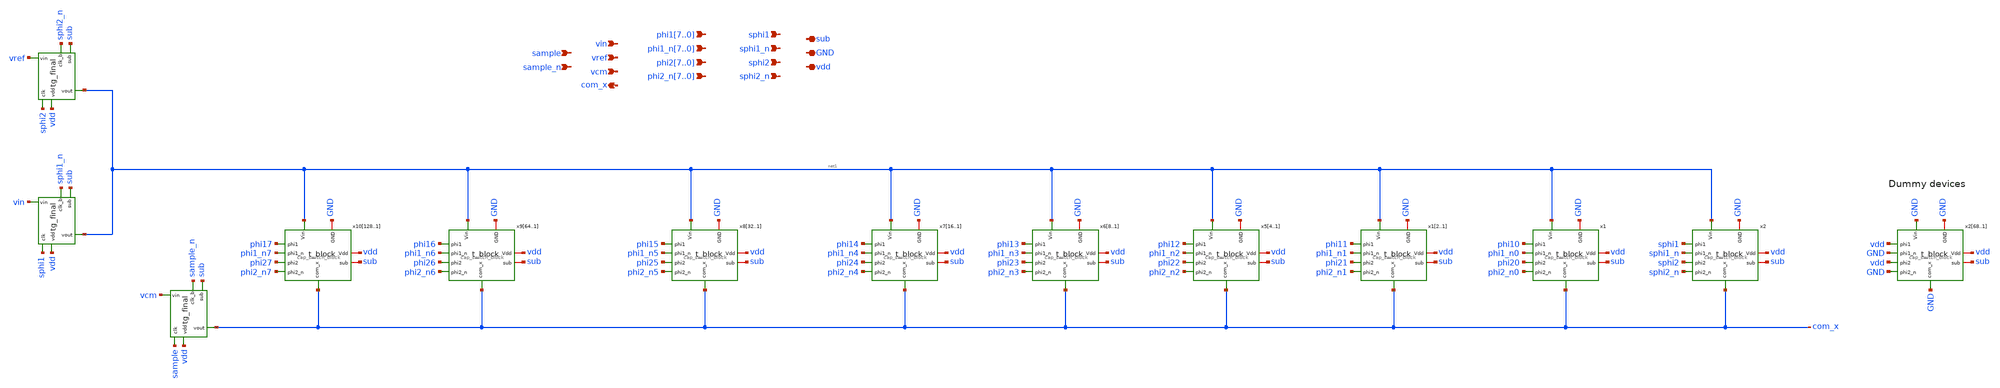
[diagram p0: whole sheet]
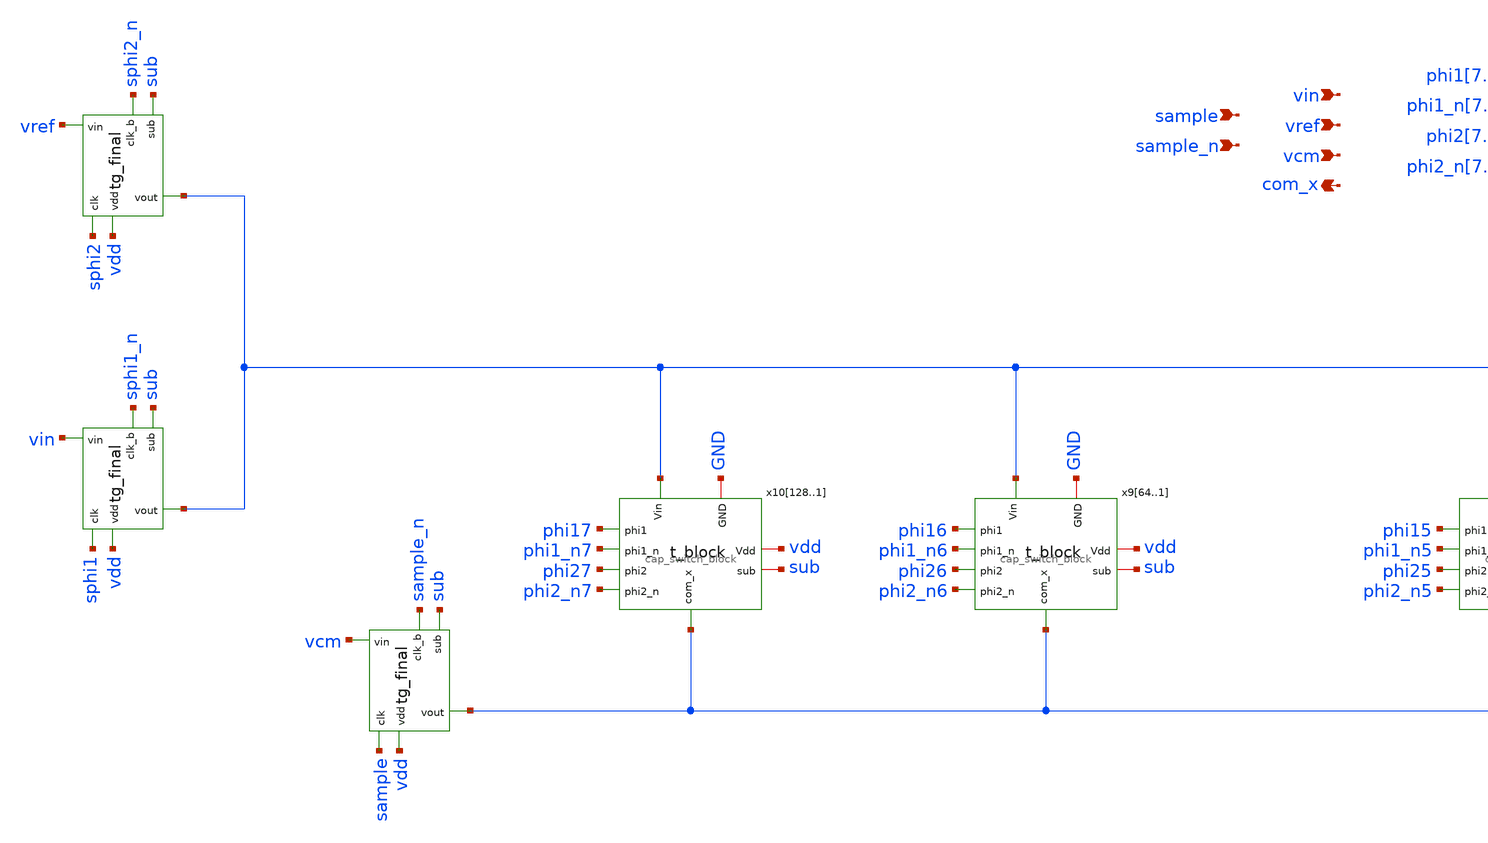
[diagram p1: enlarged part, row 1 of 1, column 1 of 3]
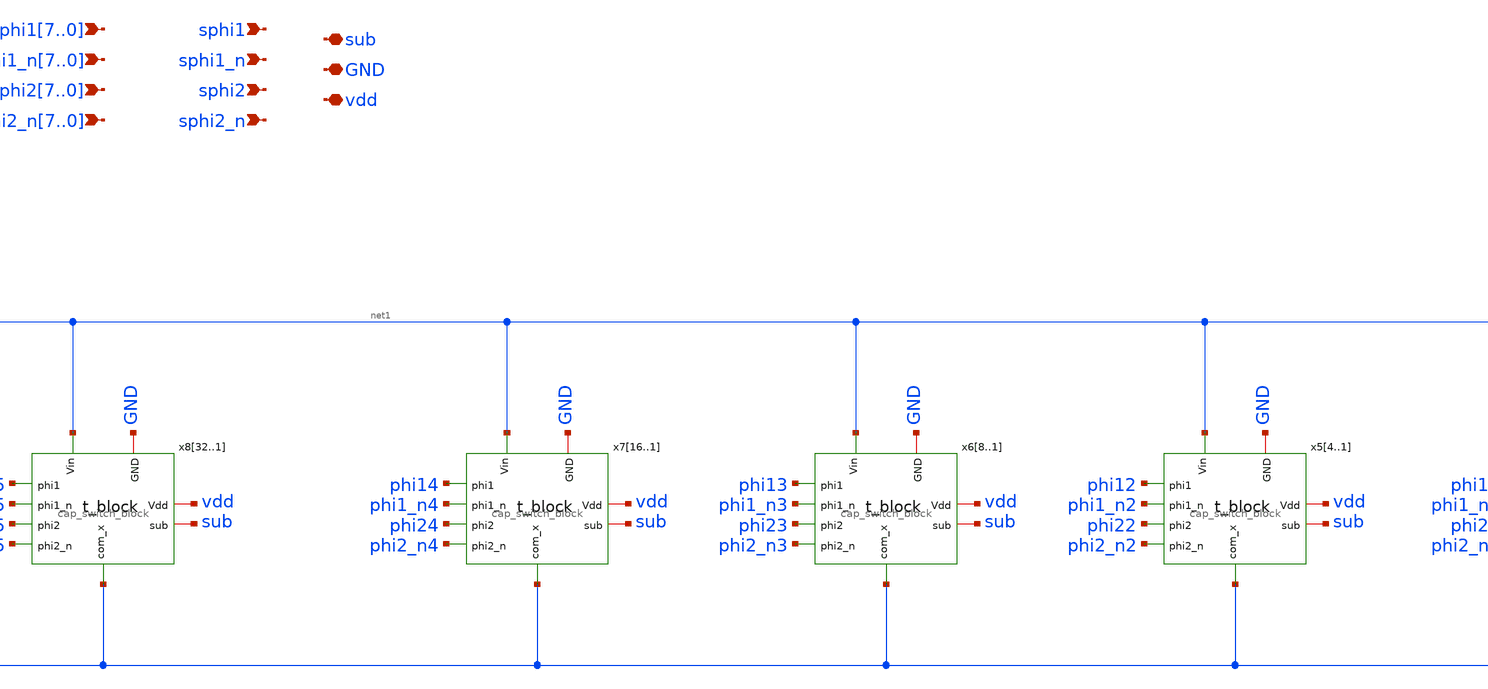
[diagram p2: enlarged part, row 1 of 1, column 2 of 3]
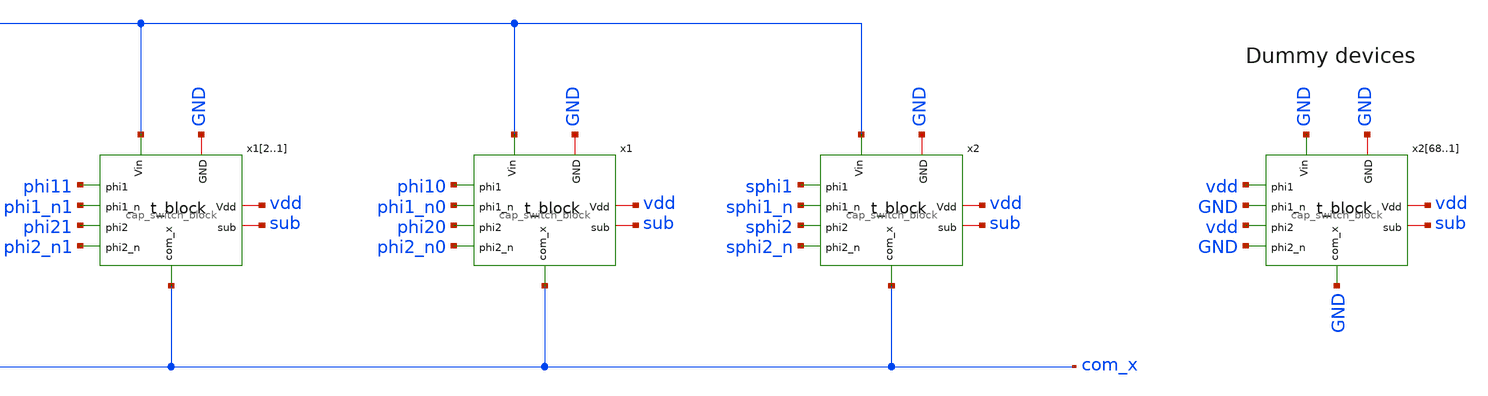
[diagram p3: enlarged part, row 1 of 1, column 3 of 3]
** sch_path: top/test/design/capdac_p.sch
**.subckt capdac_p phi17,phi16,phi15,phi14,phi13,phi12,phi11,phi10
*+ phi1_n7,phi1_n6,phi1_n5,phi1_n4,phi1_n3,phi1_n2,phi1_n1,phi1_n0 vdd GND sub phi27,phi26,phi25,phi24,phi23,phi22,phi21,phi20
*+ phi2_n7,phi2_n6,phi2_n5,phi2_n4,phi2_n3,phi2_n2,phi2_n1,phi2_n0 com_x sphi1 sphi1_n sphi2 sphi2_n vcm vref vin sample_n sample
*.ipin phi17,phi16,phi15,phi14,phi13,phi12,phi11,phi10
*.ipin phi1_n7,phi1_n6,phi1_n5,phi1_n4,phi1_n3,phi1_n2,phi1_n1,phi1_n0
*.iopin vdd
*.iopin GND
*.iopin sub
*.ipin phi27,phi26,phi25,phi24,phi23,phi22,phi21,phi20
*.ipin phi2_n7,phi2_n6,phi2_n5,phi2_n4,phi2_n3,phi2_n2,phi2_n1,phi2_n0
*.opin com_x
*.ipin sphi1
*.ipin sphi1_n
*.ipin sphi2
*.ipin sphi2_n
*.ipin vcm
*.ipin vref
*.ipin vin
*.ipin sample_n
*.ipin sample
x2 net1 sub GND vdd sphi1 sphi2 sphi2_n sphi1_n com_x cap_switch_block
x1 net1 sub GND vdd phi10 phi20 phi2_n0 phi1_n0 com_x cap_switch_block
x12 net1 sub GND vdd phi11 phi21 phi2_n1 phi1_n1 com_x cap_switch_block
x11 net1 sub GND vdd phi11 phi21 phi2_n1 phi1_n1 com_x cap_switch_block
x54 net1 sub GND vdd phi12 phi22 phi2_n2 phi1_n2 com_x cap_switch_block
x53 net1 sub GND vdd phi12 phi22 phi2_n2 phi1_n2 com_x cap_switch_block
x52 net1 sub GND vdd phi12 phi22 phi2_n2 phi1_n2 com_x cap_switch_block
x51 net1 sub GND vdd phi12 phi22 phi2_n2 phi1_n2 com_x cap_switch_block
x68 net1 sub GND vdd phi13 phi23 phi2_n3 phi1_n3 com_x cap_switch_block
x67 net1 sub GND vdd phi13 phi23 phi2_n3 phi1_n3 com_x cap_switch_block
x66 net1 sub GND vdd phi13 phi23 phi2_n3 phi1_n3 com_x cap_switch_block
x65 net1 sub GND vdd phi13 phi23 phi2_n3 phi1_n3 com_x cap_switch_block
x64 net1 sub GND vdd phi13 phi23 phi2_n3 phi1_n3 com_x cap_switch_block
x63 net1 sub GND vdd phi13 phi23 phi2_n3 phi1_n3 com_x cap_switch_block
x62 net1 sub GND vdd phi13 phi23 phi2_n3 phi1_n3 com_x cap_switch_block
x61 net1 sub GND vdd phi13 phi23 phi2_n3 phi1_n3 com_x cap_switch_block
x716 net1 sub GND vdd phi14 phi24 phi2_n4 phi1_n4 com_x cap_switch_block
x715 net1 sub GND vdd phi14 phi24 phi2_n4 phi1_n4 com_x cap_switch_block
x714 net1 sub GND vdd phi14 phi24 phi2_n4 phi1_n4 com_x cap_switch_block
x713 net1 sub GND vdd phi14 phi24 phi2_n4 phi1_n4 com_x cap_switch_block
x712 net1 sub GND vdd phi14 phi24 phi2_n4 phi1_n4 com_x cap_switch_block
x711 net1 sub GND vdd phi14 phi24 phi2_n4 phi1_n4 com_x cap_switch_block
x710 net1 sub GND vdd phi14 phi24 phi2_n4 phi1_n4 com_x cap_switch_block
x79 net1 sub GND vdd phi14 phi24 phi2_n4 phi1_n4 com_x cap_switch_block
x78 net1 sub GND vdd phi14 phi24 phi2_n4 phi1_n4 com_x cap_switch_block
x77 net1 sub GND vdd phi14 phi24 phi2_n4 phi1_n4 com_x cap_switch_block
x76 net1 sub GND vdd phi14 phi24 phi2_n4 phi1_n4 com_x cap_switch_block
x75 net1 sub GND vdd phi14 phi24 phi2_n4 phi1_n4 com_x cap_switch_block
x74 net1 sub GND vdd phi14 phi24 phi2_n4 phi1_n4 com_x cap_switch_block
x73 net1 sub GND vdd phi14 phi24 phi2_n4 phi1_n4 com_x cap_switch_block
x72 net1 sub GND vdd phi14 phi24 phi2_n4 phi1_n4 com_x cap_switch_block
x71 net1 sub GND vdd phi14 phi24 phi2_n4 phi1_n4 com_x cap_switch_block
x832 net1 sub GND vdd phi15 phi25 phi2_n5 phi1_n5 com_x cap_switch_block
x831 net1 sub GND vdd phi15 phi25 phi2_n5 phi1_n5 com_x cap_switch_block
x830 net1 sub GND vdd phi15 phi25 phi2_n5 phi1_n5 com_x cap_switch_block
x829 net1 sub GND vdd phi15 phi25 phi2_n5 phi1_n5 com_x cap_switch_block
x828 net1 sub GND vdd phi15 phi25 phi2_n5 phi1_n5 com_x cap_switch_block
x827 net1 sub GND vdd phi15 phi25 phi2_n5 phi1_n5 com_x cap_switch_block
x826 net1 sub GND vdd phi15 phi25 phi2_n5 phi1_n5 com_x cap_switch_block
x825 net1 sub GND vdd phi15 phi25 phi2_n5 phi1_n5 com_x cap_switch_block
x824 net1 sub GND vdd phi15 phi25 phi2_n5 phi1_n5 com_x cap_switch_block
x823 net1 sub GND vdd phi15 phi25 phi2_n5 phi1_n5 com_x cap_switch_block
x822 net1 sub GND vdd phi15 phi25 phi2_n5 phi1_n5 com_x cap_switch_block
x821 net1 sub GND vdd phi15 phi25 phi2_n5 phi1_n5 com_x cap_switch_block
x820 net1 sub GND vdd phi15 phi25 phi2_n5 phi1_n5 com_x cap_switch_block
x819 net1 sub GND vdd phi15 phi25 phi2_n5 phi1_n5 com_x cap_switch_block
x818 net1 sub GND vdd phi15 phi25 phi2_n5 phi1_n5 com_x cap_switch_block
x817 net1 sub GND vdd phi15 phi25 phi2_n5 phi1_n5 com_x cap_switch_block
x816 net1 sub GND vdd phi15 phi25 phi2_n5 phi1_n5 com_x cap_switch_block
x815 net1 sub GND vdd phi15 phi25 phi2_n5 phi1_n5 com_x cap_switch_block
x814 net1 sub GND vdd phi15 phi25 phi2_n5 phi1_n5 com_x cap_switch_block
x813 net1 sub GND vdd phi15 phi25 phi2_n5 phi1_n5 com_x cap_switch_block
x812 net1 sub GND vdd phi15 phi25 phi2_n5 phi1_n5 com_x cap_switch_block
x811 net1 sub GND vdd phi15 phi25 phi2_n5 phi1_n5 com_x cap_switch_block
x810 net1 sub GND vdd phi15 phi25 phi2_n5 phi1_n5 com_x cap_switch_block
x89 net1 sub GND vdd phi15 phi25 phi2_n5 phi1_n5 com_x cap_switch_block
x88 net1 sub GND vdd phi15 phi25 phi2_n5 phi1_n5 com_x cap_switch_block
x87 net1 sub GND vdd phi15 phi25 phi2_n5 phi1_n5 com_x cap_switch_block
x86 net1 sub GND vdd phi15 phi25 phi2_n5 phi1_n5 com_x cap_switch_block
x85 net1 sub GND vdd phi15 phi25 phi2_n5 phi1_n5 com_x cap_switch_block
x84 net1 sub GND vdd phi15 phi25 phi2_n5 phi1_n5 com_x cap_switch_block
x83 net1 sub GND vdd phi15 phi25 phi2_n5 phi1_n5 com_x cap_switch_block
x82 net1 sub GND vdd phi15 phi25 phi2_n5 phi1_n5 com_x cap_switch_block
x81 net1 sub GND vdd phi15 phi25 phi2_n5 phi1_n5 com_x cap_switch_block
x964 net1 sub GND vdd phi16 phi26 phi2_n6 phi1_n6 com_x cap_switch_block
x963 net1 sub GND vdd phi16 phi26 phi2_n6 phi1_n6 com_x cap_switch_block
x962 net1 sub GND vdd phi16 phi26 phi2_n6 phi1_n6 com_x cap_switch_block
x961 net1 sub GND vdd phi16 phi26 phi2_n6 phi1_n6 com_x cap_switch_block
x960 net1 sub GND vdd phi16 phi26 phi2_n6 phi1_n6 com_x cap_switch_block
x959 net1 sub GND vdd phi16 phi26 phi2_n6 phi1_n6 com_x cap_switch_block
x958 net1 sub GND vdd phi16 phi26 phi2_n6 phi1_n6 com_x cap_switch_block
x957 net1 sub GND vdd phi16 phi26 phi2_n6 phi1_n6 com_x cap_switch_block
x956 net1 sub GND vdd phi16 phi26 phi2_n6 phi1_n6 com_x cap_switch_block
x955 net1 sub GND vdd phi16 phi26 phi2_n6 phi1_n6 com_x cap_switch_block
x954 net1 sub GND vdd phi16 phi26 phi2_n6 phi1_n6 com_x cap_switch_block
x953 net1 sub GND vdd phi16 phi26 phi2_n6 phi1_n6 com_x cap_switch_block
x952 net1 sub GND vdd phi16 phi26 phi2_n6 phi1_n6 com_x cap_switch_block
x951 net1 sub GND vdd phi16 phi26 phi2_n6 phi1_n6 com_x cap_switch_block
x950 net1 sub GND vdd phi16 phi26 phi2_n6 phi1_n6 com_x cap_switch_block
x949 net1 sub GND vdd phi16 phi26 phi2_n6 phi1_n6 com_x cap_switch_block
x948 net1 sub GND vdd phi16 phi26 phi2_n6 phi1_n6 com_x cap_switch_block
x947 net1 sub GND vdd phi16 phi26 phi2_n6 phi1_n6 com_x cap_switch_block
x946 net1 sub GND vdd phi16 phi26 phi2_n6 phi1_n6 com_x cap_switch_block
x945 net1 sub GND vdd phi16 phi26 phi2_n6 phi1_n6 com_x cap_switch_block
x944 net1 sub GND vdd phi16 phi26 phi2_n6 phi1_n6 com_x cap_switch_block
x943 net1 sub GND vdd phi16 phi26 phi2_n6 phi1_n6 com_x cap_switch_block
x942 net1 sub GND vdd phi16 phi26 phi2_n6 phi1_n6 com_x cap_switch_block
x941 net1 sub GND vdd phi16 phi26 phi2_n6 phi1_n6 com_x cap_switch_block
x940 net1 sub GND vdd phi16 phi26 phi2_n6 phi1_n6 com_x cap_switch_block
x939 net1 sub GND vdd phi16 phi26 phi2_n6 phi1_n6 com_x cap_switch_block
x938 net1 sub GND vdd phi16 phi26 phi2_n6 phi1_n6 com_x cap_switch_block
x937 net1 sub GND vdd phi16 phi26 phi2_n6 phi1_n6 com_x cap_switch_block
x936 net1 sub GND vdd phi16 phi26 phi2_n6 phi1_n6 com_x cap_switch_block
x935 net1 sub GND vdd phi16 phi26 phi2_n6 phi1_n6 com_x cap_switch_block
x934 net1 sub GND vdd phi16 phi26 phi2_n6 phi1_n6 com_x cap_switch_block
x933 net1 sub GND vdd phi16 phi26 phi2_n6 phi1_n6 com_x cap_switch_block
x932 net1 sub GND vdd phi16 phi26 phi2_n6 phi1_n6 com_x cap_switch_block
x931 net1 sub GND vdd phi16 phi26 phi2_n6 phi1_n6 com_x cap_switch_block
x930 net1 sub GND vdd phi16 phi26 phi2_n6 phi1_n6 com_x cap_switch_block
x929 net1 sub GND vdd phi16 phi26 phi2_n6 phi1_n6 com_x cap_switch_block
x928 net1 sub GND vdd phi16 phi26 phi2_n6 phi1_n6 com_x cap_switch_block
x927 net1 sub GND vdd phi16 phi26 phi2_n6 phi1_n6 com_x cap_switch_block
x926 net1 sub GND vdd phi16 phi26 phi2_n6 phi1_n6 com_x cap_switch_block
x925 net1 sub GND vdd phi16 phi26 phi2_n6 phi1_n6 com_x cap_switch_block
x924 net1 sub GND vdd phi16 phi26 phi2_n6 phi1_n6 com_x cap_switch_block
x923 net1 sub GND vdd phi16 phi26 phi2_n6 phi1_n6 com_x cap_switch_block
x922 net1 sub GND vdd phi16 phi26 phi2_n6 phi1_n6 com_x cap_switch_block
x921 net1 sub GND vdd phi16 phi26 phi2_n6 phi1_n6 com_x cap_switch_block
x920 net1 sub GND vdd phi16 phi26 phi2_n6 phi1_n6 com_x cap_switch_block
x919 net1 sub GND vdd phi16 phi26 phi2_n6 phi1_n6 com_x cap_switch_block
x918 net1 sub GND vdd phi16 phi26 phi2_n6 phi1_n6 com_x cap_switch_block
x917 net1 sub GND vdd phi16 phi26 phi2_n6 phi1_n6 com_x cap_switch_block
x916 net1 sub GND vdd phi16 phi26 phi2_n6 phi1_n6 com_x cap_switch_block
x915 net1 sub GND vdd phi16 phi26 phi2_n6 phi1_n6 com_x cap_switch_block
x914 net1 sub GND vdd phi16 phi26 phi2_n6 phi1_n6 com_x cap_switch_block
x913 net1 sub GND vdd phi16 phi26 phi2_n6 phi1_n6 com_x cap_switch_block
x912 net1 sub GND vdd phi16 phi26 phi2_n6 phi1_n6 com_x cap_switch_block
x911 net1 sub GND vdd phi16 phi26 phi2_n6 phi1_n6 com_x cap_switch_block
x910 net1 sub GND vdd phi16 phi26 phi2_n6 phi1_n6 com_x cap_switch_block
x99 net1 sub GND vdd phi16 phi26 phi2_n6 phi1_n6 com_x cap_switch_block
x98 net1 sub GND vdd phi16 phi26 phi2_n6 phi1_n6 com_x cap_switch_block
x97 net1 sub GND vdd phi16 phi26 phi2_n6 phi1_n6 com_x cap_switch_block
x96 net1 sub GND vdd phi16 phi26 phi2_n6 phi1_n6 com_x cap_switch_block
x95 net1 sub GND vdd phi16 phi26 phi2_n6 phi1_n6 com_x cap_switch_block
x94 net1 sub GND vdd phi16 phi26 phi2_n6 phi1_n6 com_x cap_switch_block
x93 net1 sub GND vdd phi16 phi26 phi2_n6 phi1_n6 com_x cap_switch_block
x92 net1 sub GND vdd phi16 phi26 phi2_n6 phi1_n6 com_x cap_switch_block
x91 net1 sub GND vdd phi16 phi26 phi2_n6 phi1_n6 com_x cap_switch_block
x10128 net1 sub GND vdd phi17 phi27 phi2_n7 phi1_n7 com_x cap_switch_block
x10127 net1 sub GND vdd phi17 phi27 phi2_n7 phi1_n7 com_x cap_switch_block
x10126 net1 sub GND vdd phi17 phi27 phi2_n7 phi1_n7 com_x cap_switch_block
x10125 net1 sub GND vdd phi17 phi27 phi2_n7 phi1_n7 com_x cap_switch_block
x10124 net1 sub GND vdd phi17 phi27 phi2_n7 phi1_n7 com_x cap_switch_block
x10123 net1 sub GND vdd phi17 phi27 phi2_n7 phi1_n7 com_x cap_switch_block
x10122 net1 sub GND vdd phi17 phi27 phi2_n7 phi1_n7 com_x cap_switch_block
x10121 net1 sub GND vdd phi17 phi27 phi2_n7 phi1_n7 com_x cap_switch_block
x10120 net1 sub GND vdd phi17 phi27 phi2_n7 phi1_n7 com_x cap_switch_block
x10119 net1 sub GND vdd phi17 phi27 phi2_n7 phi1_n7 com_x cap_switch_block
x10118 net1 sub GND vdd phi17 phi27 phi2_n7 phi1_n7 com_x cap_switch_block
x10117 net1 sub GND vdd phi17 phi27 phi2_n7 phi1_n7 com_x cap_switch_block
x10116 net1 sub GND vdd phi17 phi27 phi2_n7 phi1_n7 com_x cap_switch_block
x10115 net1 sub GND vdd phi17 phi27 phi2_n7 phi1_n7 com_x cap_switch_block
x10114 net1 sub GND vdd phi17 phi27 phi2_n7 phi1_n7 com_x cap_switch_block
x10113 net1 sub GND vdd phi17 phi27 phi2_n7 phi1_n7 com_x cap_switch_block
x10112 net1 sub GND vdd phi17 phi27 phi2_n7 phi1_n7 com_x cap_switch_block
x10111 net1 sub GND vdd phi17 phi27 phi2_n7 phi1_n7 com_x cap_switch_block
x10110 net1 sub GND vdd phi17 phi27 phi2_n7 phi1_n7 com_x cap_switch_block
x10109 net1 sub GND vdd phi17 phi27 phi2_n7 phi1_n7 com_x cap_switch_block
x10108 net1 sub GND vdd phi17 phi27 phi2_n7 phi1_n7 com_x cap_switch_block
x10107 net1 sub GND vdd phi17 phi27 phi2_n7 phi1_n7 com_x cap_switch_block
x10106 net1 sub GND vdd phi17 phi27 phi2_n7 phi1_n7 com_x cap_switch_block
x10105 net1 sub GND vdd phi17 phi27 phi2_n7 phi1_n7 com_x cap_switch_block
x10104 net1 sub GND vdd phi17 phi27 phi2_n7 phi1_n7 com_x cap_switch_block
x10103 net1 sub GND vdd phi17 phi27 phi2_n7 phi1_n7 com_x cap_switch_block
x10102 net1 sub GND vdd phi17 phi27 phi2_n7 phi1_n7 com_x cap_switch_block
x10101 net1 sub GND vdd phi17 phi27 phi2_n7 phi1_n7 com_x cap_switch_block
x10100 net1 sub GND vdd phi17 phi27 phi2_n7 phi1_n7 com_x cap_switch_block
x1099 net1 sub GND vdd phi17 phi27 phi2_n7 phi1_n7 com_x cap_switch_block
x1098 net1 sub GND vdd phi17 phi27 phi2_n7 phi1_n7 com_x cap_switch_block
x1097 net1 sub GND vdd phi17 phi27 phi2_n7 phi1_n7 com_x cap_switch_block
x1096 net1 sub GND vdd phi17 phi27 phi2_n7 phi1_n7 com_x cap_switch_block
x1095 net1 sub GND vdd phi17 phi27 phi2_n7 phi1_n7 com_x cap_switch_block
x1094 net1 sub GND vdd phi17 phi27 phi2_n7 phi1_n7 com_x cap_switch_block
x1093 net1 sub GND vdd phi17 phi27 phi2_n7 phi1_n7 com_x cap_switch_block
x1092 net1 sub GND vdd phi17 phi27 phi2_n7 phi1_n7 com_x cap_switch_block
x1091 net1 sub GND vdd phi17 phi27 phi2_n7 phi1_n7 com_x cap_switch_block
x1090 net1 sub GND vdd phi17 phi27 phi2_n7 phi1_n7 com_x cap_switch_block
x1089 net1 sub GND vdd phi17 phi27 phi2_n7 phi1_n7 com_x cap_switch_block
x1088 net1 sub GND vdd phi17 phi27 phi2_n7 phi1_n7 com_x cap_switch_block
x1087 net1 sub GND vdd phi17 phi27 phi2_n7 phi1_n7 com_x cap_switch_block
x1086 net1 sub GND vdd phi17 phi27 phi2_n7 phi1_n7 com_x cap_switch_block
x1085 net1 sub GND vdd phi17 phi27 phi2_n7 phi1_n7 com_x cap_switch_block
x1084 net1 sub GND vdd phi17 phi27 phi2_n7 phi1_n7 com_x cap_switch_block
x1083 net1 sub GND vdd phi17 phi27 phi2_n7 phi1_n7 com_x cap_switch_block
x1082 net1 sub GND vdd phi17 phi27 phi2_n7 phi1_n7 com_x cap_switch_block
x1081 net1 sub GND vdd phi17 phi27 phi2_n7 phi1_n7 com_x cap_switch_block
x1080 net1 sub GND vdd phi17 phi27 phi2_n7 phi1_n7 com_x cap_switch_block
x1079 net1 sub GND vdd phi17 phi27 phi2_n7 phi1_n7 com_x cap_switch_block
x1078 net1 sub GND vdd phi17 phi27 phi2_n7 phi1_n7 com_x cap_switch_block
x1077 net1 sub GND vdd phi17 phi27 phi2_n7 phi1_n7 com_x cap_switch_block
x1076 net1 sub GND vdd phi17 phi27 phi2_n7 phi1_n7 com_x cap_switch_block
x1075 net1 sub GND vdd phi17 phi27 phi2_n7 phi1_n7 com_x cap_switch_block
x1074 net1 sub GND vdd phi17 phi27 phi2_n7 phi1_n7 com_x cap_switch_block
x1073 net1 sub GND vdd phi17 phi27 phi2_n7 phi1_n7 com_x cap_switch_block
x1072 net1 sub GND vdd phi17 phi27 phi2_n7 phi1_n7 com_x cap_switch_block
x1071 net1 sub GND vdd phi17 phi27 phi2_n7 phi1_n7 com_x cap_switch_block
x1070 net1 sub GND vdd phi17 phi27 phi2_n7 phi1_n7 com_x cap_switch_block
x1069 net1 sub GND vdd phi17 phi27 phi2_n7 phi1_n7 com_x cap_switch_block
x1068 net1 sub GND vdd phi17 phi27 phi2_n7 phi1_n7 com_x cap_switch_block
x1067 net1 sub GND vdd phi17 phi27 phi2_n7 phi1_n7 com_x cap_switch_block
x1066 net1 sub GND vdd phi17 phi27 phi2_n7 phi1_n7 com_x cap_switch_block
x1065 net1 sub GND vdd phi17 phi27 phi2_n7 phi1_n7 com_x cap_switch_block
x1064 net1 sub GND vdd phi17 phi27 phi2_n7 phi1_n7 com_x cap_switch_block
x1063 net1 sub GND vdd phi17 phi27 phi2_n7 phi1_n7 com_x cap_switch_block
x1062 net1 sub GND vdd phi17 phi27 phi2_n7 phi1_n7 com_x cap_switch_block
x1061 net1 sub GND vdd phi17 phi27 phi2_n7 phi1_n7 com_x cap_switch_block
x1060 net1 sub GND vdd phi17 phi27 phi2_n7 phi1_n7 com_x cap_switch_block
x1059 net1 sub GND vdd phi17 phi27 phi2_n7 phi1_n7 com_x cap_switch_block
x1058 net1 sub GND vdd phi17 phi27 phi2_n7 phi1_n7 com_x cap_switch_block
x1057 net1 sub GND vdd phi17 phi27 phi2_n7 phi1_n7 com_x cap_switch_block
x1056 net1 sub GND vdd phi17 phi27 phi2_n7 phi1_n7 com_x cap_switch_block
x1055 net1 sub GND vdd phi17 phi27 phi2_n7 phi1_n7 com_x cap_switch_block
x1054 net1 sub GND vdd phi17 phi27 phi2_n7 phi1_n7 com_x cap_switch_block
x1053 net1 sub GND vdd phi17 phi27 phi2_n7 phi1_n7 com_x cap_switch_block
x1052 net1 sub GND vdd phi17 phi27 phi2_n7 phi1_n7 com_x cap_switch_block
x1051 net1 sub GND vdd phi17 phi27 phi2_n7 phi1_n7 com_x cap_switch_block
x1050 net1 sub GND vdd phi17 phi27 phi2_n7 phi1_n7 com_x cap_switch_block
x1049 net1 sub GND vdd phi17 phi27 phi2_n7 phi1_n7 com_x cap_switch_block
x1048 net1 sub GND vdd phi17 phi27 phi2_n7 phi1_n7 com_x cap_switch_block
x1047 net1 sub GND vdd phi17 phi27 phi2_n7 phi1_n7 com_x cap_switch_block
x1046 net1 sub GND vdd phi17 phi27 phi2_n7 phi1_n7 com_x cap_switch_block
x1045 net1 sub GND vdd phi17 phi27 phi2_n7 phi1_n7 com_x cap_switch_block
x1044 net1 sub GND vdd phi17 phi27 phi2_n7 phi1_n7 com_x cap_switch_block
x1043 net1 sub GND vdd phi17 phi27 phi2_n7 phi1_n7 com_x cap_switch_block
x1042 net1 sub GND vdd phi17 phi27 phi2_n7 phi1_n7 com_x cap_switch_block
x1041 net1 sub GND vdd phi17 phi27 phi2_n7 phi1_n7 com_x cap_switch_block
x1040 net1 sub GND vdd phi17 phi27 phi2_n7 phi1_n7 com_x cap_switch_block
x1039 net1 sub GND vdd phi17 phi27 phi2_n7 phi1_n7 com_x cap_switch_block
x1038 net1 sub GND vdd phi17 phi27 phi2_n7 phi1_n7 com_x cap_switch_block
x1037 net1 sub GND vdd phi17 phi27 phi2_n7 phi1_n7 com_x cap_switch_block
x1036 net1 sub GND vdd phi17 phi27 phi2_n7 phi1_n7 com_x cap_switch_block
x1035 net1 sub GND vdd phi17 phi27 phi2_n7 phi1_n7 com_x cap_switch_block
x1034 net1 sub GND vdd phi17 phi27 phi2_n7 phi1_n7 com_x cap_switch_block
x1033 net1 sub GND vdd phi17 phi27 phi2_n7 phi1_n7 com_x cap_switch_block
x1032 net1 sub GND vdd phi17 phi27 phi2_n7 phi1_n7 com_x cap_switch_block
x1031 net1 sub GND vdd phi17 phi27 phi2_n7 phi1_n7 com_x cap_switch_block
x1030 net1 sub GND vdd phi17 phi27 phi2_n7 phi1_n7 com_x cap_switch_block
x1029 net1 sub GND vdd phi17 phi27 phi2_n7 phi1_n7 com_x cap_switch_block
x1028 net1 sub GND vdd phi17 phi27 phi2_n7 phi1_n7 com_x cap_switch_block
x1027 net1 sub GND vdd phi17 phi27 phi2_n7 phi1_n7 com_x cap_switch_block
x1026 net1 sub GND vdd phi17 phi27 phi2_n7 phi1_n7 com_x cap_switch_block
x1025 net1 sub GND vdd phi17 phi27 phi2_n7 phi1_n7 com_x cap_switch_block
x1024 net1 sub GND vdd phi17 phi27 phi2_n7 phi1_n7 com_x cap_switch_block
x1023 net1 sub GND vdd phi17 phi27 phi2_n7 phi1_n7 com_x cap_switch_block
x1022 net1 sub GND vdd phi17 phi27 phi2_n7 phi1_n7 com_x cap_switch_block
x1021 net1 sub GND vdd phi17 phi27 phi2_n7 phi1_n7 com_x cap_switch_block
x1020 net1 sub GND vdd phi17 phi27 phi2_n7 phi1_n7 com_x cap_switch_block
x1019 net1 sub GND vdd phi17 phi27 phi2_n7 phi1_n7 com_x cap_switch_block
x1018 net1 sub GND vdd phi17 phi27 phi2_n7 phi1_n7 com_x cap_switch_block
x1017 net1 sub GND vdd phi17 phi27 phi2_n7 phi1_n7 com_x cap_switch_block
x1016 net1 sub GND vdd phi17 phi27 phi2_n7 phi1_n7 com_x cap_switch_block
x1015 net1 sub GND vdd phi17 phi27 phi2_n7 phi1_n7 com_x cap_switch_block
x1014 net1 sub GND vdd phi17 phi27 phi2_n7 phi1_n7 com_x cap_switch_block
x1013 net1 sub GND vdd phi17 phi27 phi2_n7 phi1_n7 com_x cap_switch_block
x1012 net1 sub GND vdd phi17 phi27 phi2_n7 phi1_n7 com_x cap_switch_block
x1011 net1 sub GND vdd phi17 phi27 phi2_n7 phi1_n7 com_x cap_switch_block
x1010 net1 sub GND vdd phi17 phi27 phi2_n7 phi1_n7 com_x cap_switch_block
x109 net1 sub GND vdd phi17 phi27 phi2_n7 phi1_n7 com_x cap_switch_block
x108 net1 sub GND vdd phi17 phi27 phi2_n7 phi1_n7 com_x cap_switch_block
x107 net1 sub GND vdd phi17 phi27 phi2_n7 phi1_n7 com_x cap_switch_block
x106 net1 sub GND vdd phi17 phi27 phi2_n7 phi1_n7 com_x cap_switch_block
x105 net1 sub GND vdd phi17 phi27 phi2_n7 phi1_n7 com_x cap_switch_block
x104 net1 sub GND vdd phi17 phi27 phi2_n7 phi1_n7 com_x cap_switch_block
x103 net1 sub GND vdd phi17 phi27 phi2_n7 phi1_n7 com_x cap_switch_block
x102 net1 sub GND vdd phi17 phi27 phi2_n7 phi1_n7 com_x cap_switch_block
x101 net1 sub GND vdd phi17 phi27 phi2_n7 phi1_n7 com_x cap_switch_block
x5[10] sphi2 sub net1 vref vdd sphi2_n tg_final
x5[9] sphi2 sub net1 vref vdd sphi2_n tg_final
x5[8] sphi2 sub net1 vref vdd sphi2_n tg_final
x5[7] sphi2 sub net1 vref vdd sphi2_n tg_final
x5[6] sphi2 sub net1 vref vdd sphi2_n tg_final
x5[5] sphi2 sub net1 vref vdd sphi2_n tg_final
x5[4] sphi2 sub net1 vref vdd sphi2_n tg_final
x5[3] sphi2 sub net1 vref vdd sphi2_n tg_final
x5[2] sphi2 sub net1 vref vdd sphi2_n tg_final
x5[1] sphi2 sub net1 vref vdd sphi2_n tg_final
x6[10] sphi1 sub net1 vin vdd sphi1_n tg_final
x6[9] sphi1 sub net1 vin vdd sphi1_n tg_final
x6[8] sphi1 sub net1 vin vdd sphi1_n tg_final
x6[7] sphi1 sub net1 vin vdd sphi1_n tg_final
x6[6] sphi1 sub net1 vin vdd sphi1_n tg_final
x6[5] sphi1 sub net1 vin vdd sphi1_n tg_final
x6[4] sphi1 sub net1 vin vdd sphi1_n tg_final
x6[3] sphi1 sub net1 vin vdd sphi1_n tg_final
x6[2] sphi1 sub net1 vin vdd sphi1_n tg_final
x6[1] sphi1 sub net1 vin vdd sphi1_n tg_final
x3[10] sample sub com_x vcm vdd sample_n tg_final
x3[9] sample sub com_x vcm vdd sample_n tg_final
x3[8] sample sub com_x vcm vdd sample_n tg_final
x3[7] sample sub com_x vcm vdd sample_n tg_final
x3[6] sample sub com_x vcm vdd sample_n tg_final
x3[5] sample sub com_x vcm vdd sample_n tg_final
x3[4] sample sub com_x vcm vdd sample_n tg_final
x3[3] sample sub com_x vcm vdd sample_n tg_final
x3[2] sample sub com_x vcm vdd sample_n tg_final
x3[1] sample sub com_x vcm vdd sample_n tg_final
x268 GND sub GND vdd vdd vdd GND GND GND cap_switch_block
x267 GND sub GND vdd vdd vdd GND GND GND cap_switch_block
x266 GND sub GND vdd vdd vdd GND GND GND cap_switch_block
x265 GND sub GND vdd vdd vdd GND GND GND cap_switch_block
x264 GND sub GND vdd vdd vdd GND GND GND cap_switch_block
x263 GND sub GND vdd vdd vdd GND GND GND cap_switch_block
x262 GND sub GND vdd vdd vdd GND GND GND cap_switch_block
x261 GND sub GND vdd vdd vdd GND GND GND cap_switch_block
x260 GND sub GND vdd vdd vdd GND GND GND cap_switch_block
x259 GND sub GND vdd vdd vdd GND GND GND cap_switch_block
x258 GND sub GND vdd vdd vdd GND GND GND cap_switch_block
x257 GND sub GND vdd vdd vdd GND GND GND cap_switch_block
x256 GND sub GND vdd vdd vdd GND GND GND cap_switch_block
x255 GND sub GND vdd vdd vdd GND GND GND cap_switch_block
x254 GND sub GND vdd vdd vdd GND GND GND cap_switch_block
x253 GND sub GND vdd vdd vdd GND GND GND cap_switch_block
x252 GND sub GND vdd vdd vdd GND GND GND cap_switch_block
x251 GND sub GND vdd vdd vdd GND GND GND cap_switch_block
x250 GND sub GND vdd vdd vdd GND GND GND cap_switch_block
x249 GND sub GND vdd vdd vdd GND GND GND cap_switch_block
x248 GND sub GND vdd vdd vdd GND GND GND cap_switch_block
x247 GND sub GND vdd vdd vdd GND GND GND cap_switch_block
x246 GND sub GND vdd vdd vdd GND GND GND cap_switch_block
x245 GND sub GND vdd vdd vdd GND GND GND cap_switch_block
x244 GND sub GND vdd vdd vdd GND GND GND cap_switch_block
x243 GND sub GND vdd vdd vdd GND GND GND cap_switch_block
x242 GND sub GND vdd vdd vdd GND GND GND cap_switch_block
x241 GND sub GND vdd vdd vdd GND GND GND cap_switch_block
x240 GND sub GND vdd vdd vdd GND GND GND cap_switch_block
x239 GND sub GND vdd vdd vdd GND GND GND cap_switch_block
x238 GND sub GND vdd vdd vdd GND GND GND cap_switch_block
x237 GND sub GND vdd vdd vdd GND GND GND cap_switch_block
x236 GND sub GND vdd vdd vdd GND GND GND cap_switch_block
x235 GND sub GND vdd vdd vdd GND GND GND cap_switch_block
x234 GND sub GND vdd vdd vdd GND GND GND cap_switch_block
x233 GND sub GND vdd vdd vdd GND GND GND cap_switch_block
x232 GND sub GND vdd vdd vdd GND GND GND cap_switch_block
x231 GND sub GND vdd vdd vdd GND GND GND cap_switch_block
x230 GND sub GND vdd vdd vdd GND GND GND cap_switch_block
x229 GND sub GND vdd vdd vdd GND GND GND cap_switch_block
x228 GND sub GND vdd vdd vdd GND GND GND cap_switch_block
x227 GND sub GND vdd vdd vdd GND GND GND cap_switch_block
x226 GND sub GND vdd vdd vdd GND GND GND cap_switch_block
x225 GND sub GND vdd vdd vdd GND GND GND cap_switch_block
x224 GND sub GND vdd vdd vdd GND GND GND cap_switch_block
x223 GND sub GND vdd vdd vdd GND GND GND cap_switch_block
x222 GND sub GND vdd vdd vdd GND GND GND cap_switch_block
x221 GND sub GND vdd vdd vdd GND GND GND cap_switch_block
x220 GND sub GND vdd vdd vdd GND GND GND cap_switch_block
x219 GND sub GND vdd vdd vdd GND GND GND cap_switch_block
x218 GND sub GND vdd vdd vdd GND GND GND cap_switch_block
x217 GND sub GND vdd vdd vdd GND GND GND cap_switch_block
x216 GND sub GND vdd vdd vdd GND GND GND cap_switch_block
x215 GND sub GND vdd vdd vdd GND GND GND cap_switch_block
x214 GND sub GND vdd vdd vdd GND GND GND cap_switch_block
x213 GND sub GND vdd vdd vdd GND GND GND cap_switch_block
x212 GND sub GND vdd vdd vdd GND GND GND cap_switch_block
x211 GND sub GND vdd vdd vdd GND GND GND cap_switch_block
x210 GND sub GND vdd vdd vdd GND GND GND cap_switch_block
x29 GND sub GND vdd vdd vdd GND GND GND cap_switch_block
x28 GND sub GND vdd vdd vdd GND GND GND cap_switch_block
x27 GND sub GND vdd vdd vdd GND GND GND cap_switch_block
x26 GND sub GND vdd vdd vdd GND GND GND cap_switch_block
x25 GND sub GND vdd vdd vdd GND GND GND cap_switch_block
x24 GND sub GND vdd vdd vdd GND GND GND cap_switch_block
x23 GND sub GND vdd vdd vdd GND GND GND cap_switch_block
x22 GND sub GND vdd vdd vdd GND GND GND cap_switch_block
x21 GND sub GND vdd vdd vdd GND GND GND cap_switch_block
**.ends

* expanding   symbol:  /foss/designs/test/design/cap_switch_block.sym # of pins=9
** sym_path: test/design/cap_switch_block.sym
** sch_path: test/design/cap_switch_block.sch
.subckt cap_switch_block Vin sub GND Vdd phi1 phi2 phi2_n phi1_n com_x
*.ipin Vin
*.opin com_x
*.ipin phi1
*.ipin phi1_n
*.iopin Vdd
*.iopin GND
*.iopin sub
*.ipin phi2
*.ipin phi2_n
XC9 com_x net1 sky130_fd_pr__cap_mim_m3_1 W=7 L=7 MF=1 m=1
x4 phi1 sub net1 Vin Vdd phi1_n tg_final
x1 phi2 sub net1 GND Vdd phi2_n tg_final
.ends


* expanding   symbol:  /foss/designs/test/design/tg_final.sym # of pins=6
** sym_path: top/test/design/tg_final.sym
** sch_path: top/test/design/tg_final.sch
.subckt tg_final clk sub vout vin vdd clk_b
*.ipin clk
*.ipin vin
*.opin vout
*.ipin vdd
*.ipin sub
*.ipin clk_b
XM2 vout clk vin sub sky130_fd_pr__nfet_01v8 L=0.15 W=1 nf=1 ad='int((nf+1)/2) * W/nf * 0.29' as='int((nf+2)/2) * W/nf * 0.29'
+ pd='2*int((nf+1)/2) * (W/nf + 0.29)' ps='2*int((nf+2)/2) * (W/nf + 0.29)' nrd='0.29 / W' nrs='0.29 / W'
+ sa=0 sb=0 sd=0 mult=1 m=1
XM1 vout clk_b vin vdd sky130_fd_pr__pfet_01v8 L=0.15 W=1 nf=1 ad='int((nf+1)/2) * W/nf * 0.29' as='int((nf+2)/2) * W/nf * 0.29'
+ pd='2*int((nf+1)/2) * (W/nf + 0.29)' ps='2*int((nf+2)/2) * (W/nf + 0.29)' nrd='0.29 / W' nrs='0.29 / W'
+ sa=0 sb=0 sd=0 mult=1 m=1
.ends

.end
